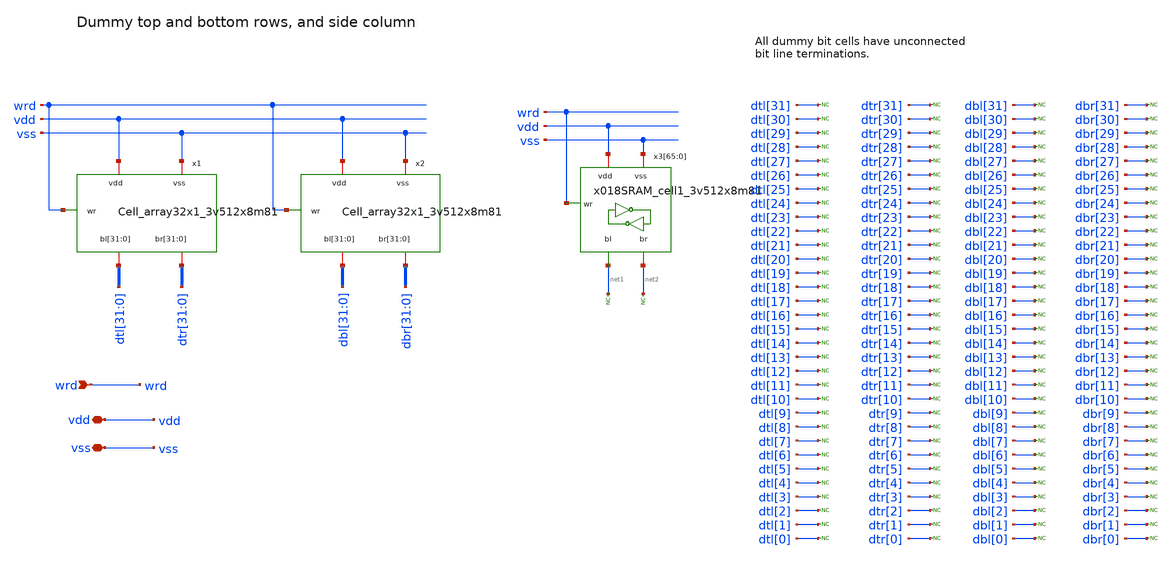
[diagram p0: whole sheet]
** sch_path: cells/gf180mcu_ocd_ip_sram__sram512x8m8wm1/xschem/ldummy_3v512x4_3v512x8m81.sch
**.subckt ldummy_3v512x4_3v512x8m81 wrd vdd vss
*.ipin wrd
*.iopin vdd
*.iopin vss
x1 dtr[31] dtr[30] dtr[29] dtr[28] dtr[27] dtr[26] dtr[25] dtr[24] dtr[23] dtr[22] dtr[21] dtr[20]
+ dtr[19] dtr[18] dtr[17] dtr[16] dtr[15] dtr[14] dtr[13] dtr[12] dtr[11] dtr[10] dtr[9] dtr[8] dtr[7] dtr[6]
+ dtr[5] dtr[4] dtr[3] dtr[2] dtr[1] dtr[0] dtl[31] dtl[30] dtl[29] dtl[28] dtl[27] dtl[26] dtl[25] dtl[24]
+ dtl[23] dtl[22] dtl[21] dtl[20] dtl[19] dtl[18] dtl[17] dtl[16] dtl[15] dtl[14] dtl[13] dtl[12] dtl[11]
+ dtl[10] dtl[9] dtl[8] dtl[7] dtl[6] dtl[5] dtl[4] dtl[3] dtl[2] dtl[1] dtl[0] vdd vss wrd
+ Cell_array32x1_3v512x8m81
x2 dbr[31] dbr[30] dbr[29] dbr[28] dbr[27] dbr[26] dbr[25] dbr[24] dbr[23] dbr[22] dbr[21] dbr[20]
+ dbr[19] dbr[18] dbr[17] dbr[16] dbr[15] dbr[14] dbr[13] dbr[12] dbr[11] dbr[10] dbr[9] dbr[8] dbr[7] dbr[6]
+ dbr[5] dbr[4] dbr[3] dbr[2] dbr[1] dbr[0] dbl[31] dbl[30] dbl[29] dbl[28] dbl[27] dbl[26] dbl[25] dbl[24]
+ dbl[23] dbl[22] dbl[21] dbl[20] dbl[19] dbl[18] dbl[17] dbl[16] dbl[15] dbl[14] dbl[13] dbl[12] dbl[11]
+ dbl[10] dbl[9] dbl[8] dbl[7] dbl[6] dbl[5] dbl[4] dbl[3] dbl[2] dbl[1] dbl[0] vdd vss wrd
+ Cell_array32x1_3v512x8m81
x3[65] vdd wrd net1 net2 vss x018SRAM_cell1_3v512x8m81
x3[64] vdd wrd net1 net2 vss x018SRAM_cell1_3v512x8m81
x3[63] vdd wrd net1 net2 vss x018SRAM_cell1_3v512x8m81
x3[62] vdd wrd net1 net2 vss x018SRAM_cell1_3v512x8m81
x3[61] vdd wrd net1 net2 vss x018SRAM_cell1_3v512x8m81
x3[60] vdd wrd net1 net2 vss x018SRAM_cell1_3v512x8m81
x3[59] vdd wrd net1 net2 vss x018SRAM_cell1_3v512x8m81
x3[58] vdd wrd net1 net2 vss x018SRAM_cell1_3v512x8m81
x3[57] vdd wrd net1 net2 vss x018SRAM_cell1_3v512x8m81
x3[56] vdd wrd net1 net2 vss x018SRAM_cell1_3v512x8m81
x3[55] vdd wrd net1 net2 vss x018SRAM_cell1_3v512x8m81
x3[54] vdd wrd net1 net2 vss x018SRAM_cell1_3v512x8m81
x3[53] vdd wrd net1 net2 vss x018SRAM_cell1_3v512x8m81
x3[52] vdd wrd net1 net2 vss x018SRAM_cell1_3v512x8m81
x3[51] vdd wrd net1 net2 vss x018SRAM_cell1_3v512x8m81
x3[50] vdd wrd net1 net2 vss x018SRAM_cell1_3v512x8m81
x3[49] vdd wrd net1 net2 vss x018SRAM_cell1_3v512x8m81
x3[48] vdd wrd net1 net2 vss x018SRAM_cell1_3v512x8m81
x3[47] vdd wrd net1 net2 vss x018SRAM_cell1_3v512x8m81
x3[46] vdd wrd net1 net2 vss x018SRAM_cell1_3v512x8m81
x3[45] vdd wrd net1 net2 vss x018SRAM_cell1_3v512x8m81
x3[44] vdd wrd net1 net2 vss x018SRAM_cell1_3v512x8m81
x3[43] vdd wrd net1 net2 vss x018SRAM_cell1_3v512x8m81
x3[42] vdd wrd net1 net2 vss x018SRAM_cell1_3v512x8m81
x3[41] vdd wrd net1 net2 vss x018SRAM_cell1_3v512x8m81
x3[40] vdd wrd net1 net2 vss x018SRAM_cell1_3v512x8m81
x3[39] vdd wrd net1 net2 vss x018SRAM_cell1_3v512x8m81
x3[38] vdd wrd net1 net2 vss x018SRAM_cell1_3v512x8m81
x3[37] vdd wrd net1 net2 vss x018SRAM_cell1_3v512x8m81
x3[36] vdd wrd net1 net2 vss x018SRAM_cell1_3v512x8m81
x3[35] vdd wrd net1 net2 vss x018SRAM_cell1_3v512x8m81
x3[34] vdd wrd net1 net2 vss x018SRAM_cell1_3v512x8m81
x3[33] vdd wrd net1 net2 vss x018SRAM_cell1_3v512x8m81
x3[32] vdd wrd net1 net2 vss x018SRAM_cell1_3v512x8m81
x3[31] vdd wrd net1 net2 vss x018SRAM_cell1_3v512x8m81
x3[30] vdd wrd net1 net2 vss x018SRAM_cell1_3v512x8m81
x3[29] vdd wrd net1 net2 vss x018SRAM_cell1_3v512x8m81
x3[28] vdd wrd net1 net2 vss x018SRAM_cell1_3v512x8m81
x3[27] vdd wrd net1 net2 vss x018SRAM_cell1_3v512x8m81
x3[26] vdd wrd net1 net2 vss x018SRAM_cell1_3v512x8m81
x3[25] vdd wrd net1 net2 vss x018SRAM_cell1_3v512x8m81
x3[24] vdd wrd net1 net2 vss x018SRAM_cell1_3v512x8m81
x3[23] vdd wrd net1 net2 vss x018SRAM_cell1_3v512x8m81
x3[22] vdd wrd net1 net2 vss x018SRAM_cell1_3v512x8m81
x3[21] vdd wrd net1 net2 vss x018SRAM_cell1_3v512x8m81
x3[20] vdd wrd net1 net2 vss x018SRAM_cell1_3v512x8m81
x3[19] vdd wrd net1 net2 vss x018SRAM_cell1_3v512x8m81
x3[18] vdd wrd net1 net2 vss x018SRAM_cell1_3v512x8m81
x3[17] vdd wrd net1 net2 vss x018SRAM_cell1_3v512x8m81
x3[16] vdd wrd net1 net2 vss x018SRAM_cell1_3v512x8m81
x3[15] vdd wrd net1 net2 vss x018SRAM_cell1_3v512x8m81
x3[14] vdd wrd net1 net2 vss x018SRAM_cell1_3v512x8m81
x3[13] vdd wrd net1 net2 vss x018SRAM_cell1_3v512x8m81
x3[12] vdd wrd net1 net2 vss x018SRAM_cell1_3v512x8m81
x3[11] vdd wrd net1 net2 vss x018SRAM_cell1_3v512x8m81
x3[10] vdd wrd net1 net2 vss x018SRAM_cell1_3v512x8m81
x3[9] vdd wrd net1 net2 vss x018SRAM_cell1_3v512x8m81
x3[8] vdd wrd net1 net2 vss x018SRAM_cell1_3v512x8m81
x3[7] vdd wrd net1 net2 vss x018SRAM_cell1_3v512x8m81
x3[6] vdd wrd net1 net2 vss x018SRAM_cell1_3v512x8m81
x3[5] vdd wrd net1 net2 vss x018SRAM_cell1_3v512x8m81
x3[4] vdd wrd net1 net2 vss x018SRAM_cell1_3v512x8m81
x3[3] vdd wrd net1 net2 vss x018SRAM_cell1_3v512x8m81
x3[2] vdd wrd net1 net2 vss x018SRAM_cell1_3v512x8m81
x3[1] vdd wrd net1 net2 vss x018SRAM_cell1_3v512x8m81
x3[0] vdd wrd net1 net2 vss x018SRAM_cell1_3v512x8m81
* noconn #net2
* noconn #net1
* noconn dtl[31]
* noconn dtl[30]
* noconn dtl[29]
* noconn dtl[28]
* noconn dtl[27]
* noconn dtl[26]
* noconn dtl[25]
* noconn dtl[24]
* noconn dtl[23]
* noconn dtl[22]
* noconn dtl[21]
* noconn dtl[20]
* noconn dtl[19]
* noconn dtl[18]
* noconn dtl[17]
* noconn dtl[16]
* noconn dtl[15]
* noconn dtl[14]
* noconn dtl[13]
* noconn dtl[12]
* noconn dtl[11]
* noconn dtl[10]
* noconn dtl[9]
* noconn dtl[8]
* noconn dtl[7]
* noconn dtl[6]
* noconn dtl[5]
* noconn dtl[4]
* noconn dtl[3]
* noconn dtl[2]
* noconn dtl[1]
* noconn dtl[0]
* noconn dtr[31]
* noconn dtr[30]
* noconn dtr[29]
* noconn dtr[28]
* noconn dtr[27]
* noconn dtr[26]
* noconn dtr[25]
* noconn dtr[24]
* noconn dtr[23]
* noconn dtr[22]
* noconn dtr[21]
* noconn dtr[20]
* noconn dtr[19]
* noconn dtr[18]
* noconn dtr[17]
* noconn dtr[16]
* noconn dtr[15]
* noconn dtr[14]
* noconn dtr[13]
* noconn dtr[12]
* noconn dtr[11]
* noconn dtr[10]
* noconn dtr[9]
* noconn dtr[8]
* noconn dtr[7]
* noconn dtr[6]
* noconn dtr[5]
* noconn dtr[4]
* noconn dtr[3]
* noconn dtr[2]
* noconn dtr[1]
* noconn dtr[0]
* noconn dbl[31]
* noconn dbl[30]
* noconn dbl[29]
* noconn dbl[28]
* noconn dbl[27]
* noconn dbl[26]
* noconn dbl[25]
* noconn dbl[24]
* noconn dbl[23]
* noconn dbl[22]
* noconn dbl[21]
* noconn dbl[20]
* noconn dbl[19]
* noconn dbl[18]
* noconn dbl[17]
* noconn dbl[16]
* noconn dbl[15]
* noconn dbl[14]
* noconn dbl[13]
* noconn dbl[12]
* noconn dbl[11]
* noconn dbl[10]
* noconn dbl[9]
* noconn dbl[8]
* noconn dbl[7]
* noconn dbl[6]
* noconn dbl[5]
* noconn dbl[4]
* noconn dbl[3]
* noconn dbl[2]
* noconn dbl[1]
* noconn dbl[0]
* noconn dbr[31]
* noconn dbr[30]
* noconn dbr[29]
* noconn dbr[28]
* noconn dbr[27]
* noconn dbr[26]
* noconn dbr[25]
* noconn dbr[24]
* noconn dbr[23]
* noconn dbr[22]
* noconn dbr[21]
* noconn dbr[20]
* noconn dbr[19]
* noconn dbr[18]
* noconn dbr[17]
* noconn dbr[16]
* noconn dbr[15]
* noconn dbr[14]
* noconn dbr[13]
* noconn dbr[12]
* noconn dbr[11]
* noconn dbr[10]
* noconn dbr[9]
* noconn dbr[8]
* noconn dbr[7]
* noconn dbr[6]
* noconn dbr[5]
* noconn dbr[4]
* noconn dbr[3]
* noconn dbr[2]
* noconn dbr[1]
* noconn dbr[0]
**.ends
.end
